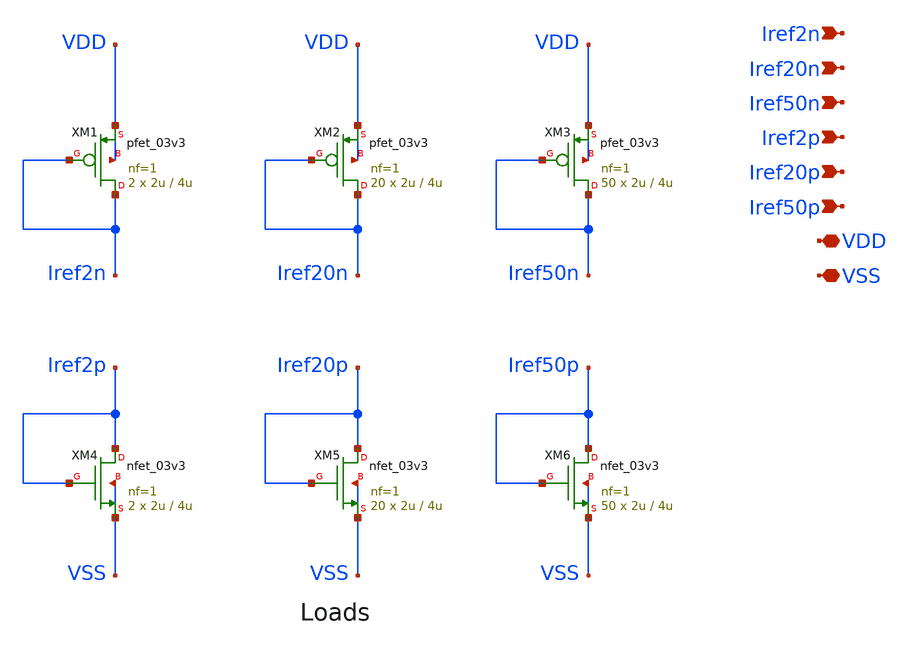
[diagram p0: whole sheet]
** sch_path: designs/libs/current_reference_load_v2/xschem/current_reference_load_v2.sch
**.subckt current_reference_load_v2 Iref2n VDD VSS Iref50n Iref2p Iref50p Iref20p Iref20n
*.ipin Iref2n
*.iopin VDD
*.iopin VSS
*.ipin Iref50n
*.ipin Iref2p
*.ipin Iref50p
*.ipin Iref20p
*.ipin Iref20n
XM1 Iref2n Iref2n VDD VDD pfet_03v3 L=4u W=2u nf=1 ad='int((nf+1)/2) * W/nf * 0.18u' as='int((nf+2)/2) * W/nf * 0.18u'
+ pd='2*int((nf+1)/2) * (W/nf + 0.18u)' ps='2*int((nf+2)/2) * (W/nf + 0.18u)' nrd='0.18u / W' nrs='0.18u / W'
+ sa=0 sb=0 sd=0 m=2
XM4 Iref2p Iref2p VSS VSS nfet_03v3 L=4u W=2u nf=1 ad='int((nf+1)/2) * W/nf * 0.18u' as='int((nf+2)/2) * W/nf * 0.18u'
+ pd='2*int((nf+1)/2) * (W/nf + 0.18u)' ps='2*int((nf+2)/2) * (W/nf + 0.18u)' nrd='0.18u / W' nrs='0.18u / W'
+ sa=0 sb=0 sd=0 m=2
XM3 Iref50n Iref50n VDD VDD pfet_03v3 L=4u W=2u nf=1 ad='int((nf+1)/2) * W/nf * 0.18u' as='int((nf+2)/2) * W/nf * 0.18u'
+ pd='2*int((nf+1)/2) * (W/nf + 0.18u)' ps='2*int((nf+2)/2) * (W/nf + 0.18u)' nrd='0.18u / W' nrs='0.18u / W'
+ sa=0 sb=0 sd=0 m=50
XM6 Iref50p Iref50p VSS VSS nfet_03v3 L=4u W=2u nf=1 ad='int((nf+1)/2) * W/nf * 0.18u' as='int((nf+2)/2) * W/nf * 0.18u'
+ pd='2*int((nf+1)/2) * (W/nf + 0.18u)' ps='2*int((nf+2)/2) * (W/nf + 0.18u)' nrd='0.18u / W' nrs='0.18u / W'
+ sa=0 sb=0 sd=0 m=50
XM2 Iref20n Iref20n VDD VDD pfet_03v3 L=4u W=2u nf=1 ad='int((nf+1)/2) * W/nf * 0.18u' as='int((nf+2)/2) * W/nf * 0.18u'
+ pd='2*int((nf+1)/2) * (W/nf + 0.18u)' ps='2*int((nf+2)/2) * (W/nf + 0.18u)' nrd='0.18u / W' nrs='0.18u / W'
+ sa=0 sb=0 sd=0 m=20
XM5 Iref20p Iref20p VSS VSS nfet_03v3 L=4u W=2u nf=1 ad='int((nf+1)/2) * W/nf * 0.18u' as='int((nf+2)/2) * W/nf * 0.18u'
+ pd='2*int((nf+1)/2) * (W/nf + 0.18u)' ps='2*int((nf+2)/2) * (W/nf + 0.18u)' nrd='0.18u / W' nrs='0.18u / W'
+ sa=0 sb=0 sd=0 m=20
**.ends
.end
